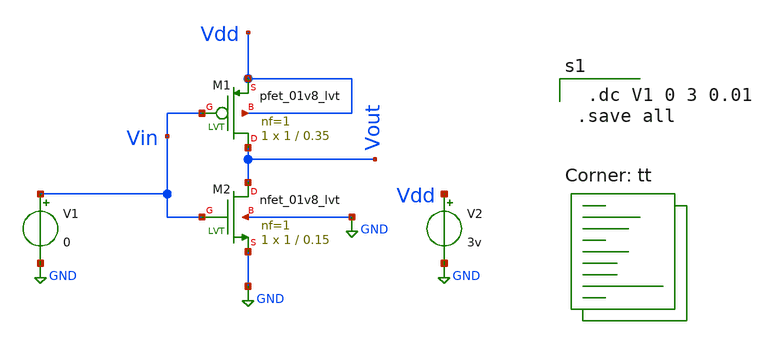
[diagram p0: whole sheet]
** sch_path: test2.sch
**.subckt test2
XM1 Vout Vin Vdd Vdd sky130_fd_pr__pfet_01v8_lvt L=0.35 W=1 nf=1 ad='int((nf+1)/2) * W/nf * 0.29' as='int((nf+2)/2) * W/nf * 0.29'
+ pd='2*int((nf+1)/2) * (W/nf + 0.29)' ps='2*int((nf+2)/2) * (W/nf + 0.29)' nrd='0.29 / W' nrs='0.29 / W'
+ sa=0 sb=0 sd=0 mult=1 m=1
XM2 Vout Vin GND GND sky130_fd_pr__nfet_01v8_lvt L=0.15 W=1 nf=1 ad='int((nf+1)/2) * W/nf * 0.29' as='int((nf+2)/2) * W/nf * 0.29'
+ pd='2*int((nf+1)/2) * (W/nf + 0.29)' ps='2*int((nf+2)/2) * (W/nf + 0.29)' nrd='0.29 / W' nrs='0.29 / W'
+ sa=0 sb=0 sd=0 mult=1 m=1
V1 Vin GND 0
V2 Vdd GND 3v
**** begin user architecture code

 .dc V1 0 3 0.01
.save all

.lib $::SKYWATER_MODELS/sky130.lib.spice tt
**** end user architecture code
**.ends
.GLOBAL GND
.end
